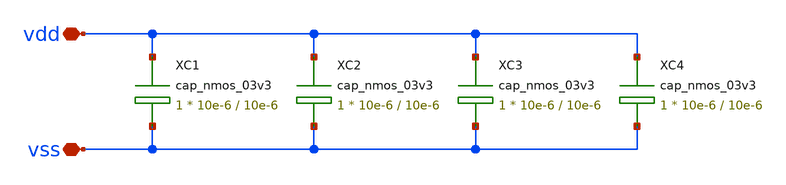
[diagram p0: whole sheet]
** sch_path: designs/libs/qw_core_analog/DECAP_SC/DECAP_SC.sch
**.subckt DECAP_SC vdd vss
*.iopin vdd
*.iopin vss
XC1 vdd vss cap_nmos_03v3 c_width=10e-6 c_length=10e-6 m=1
XC2 vdd vss cap_nmos_03v3 c_width=10e-6 c_length=10e-6 m=1
XC3 vdd vss cap_nmos_03v3 c_width=10e-6 c_length=10e-6 m=1
XC4 vdd vss cap_nmos_03v3 c_width=10e-6 c_length=10e-6 m=1
**.ends
.end
